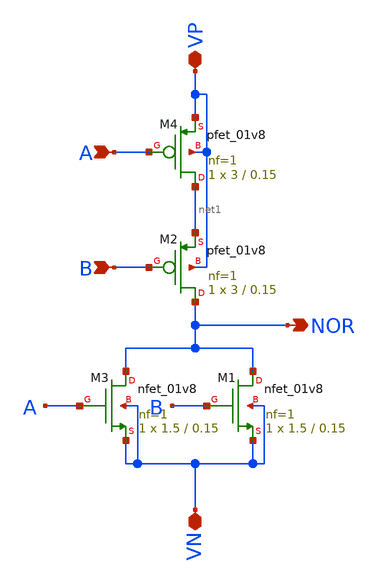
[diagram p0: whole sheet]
** sch_path: skywater_stuff/NOR_VP_VN_LVS.sch
**.subckt NOR_VP_VN_LVS A B NOR VP VN
*.ipin A
*.ipin B
*.opin NOR
*.iopin VP
*.iopin VN
XM1 NOR B VN VN sky130_fd_pr__nfet_01v8 L=0.15 W=1.5 nf=1 ad='int((nf+1)/2) * W/nf * 0.29' as='int((nf+2)/2) * W/nf * 0.29'
+ pd='2*int((nf+1)/2) * (W/nf + 0.29)' ps='2*int((nf+2)/2) * (W/nf + 0.29)' nrd='0.29 / W' nrs='0.29 / W'
+ sa=0 sb=0 sd=0 mult=1 m=1
XM3 NOR A VN VN sky130_fd_pr__nfet_01v8 L=0.15 W=1.5 nf=1 ad='int((nf+1)/2) * W/nf * 0.29' as='int((nf+2)/2) * W/nf * 0.29'
+ pd='2*int((nf+1)/2) * (W/nf + 0.29)' ps='2*int((nf+2)/2) * (W/nf + 0.29)' nrd='0.29 / W' nrs='0.29 / W'
+ sa=0 sb=0 sd=0 mult=1 m=1
XM4 net1 A VP VP sky130_fd_pr__pfet_01v8 L=0.15 W=3 nf=1 ad='int((nf+1)/2) * W/nf * 0.29' as='int((nf+2)/2) * W/nf * 0.29'
+ pd='2*int((nf+1)/2) * (W/nf + 0.29)' ps='2*int((nf+2)/2) * (W/nf + 0.29)' nrd='0.29 / W' nrs='0.29 / W'
+ sa=0 sb=0 sd=0 mult=1 m=1
XM2 NOR B net1 VP sky130_fd_pr__pfet_01v8 L=0.15 W=3 nf=1 ad='int((nf+1)/2) * W/nf * 0.29' as='int((nf+2)/2) * W/nf * 0.29'
+ pd='2*int((nf+1)/2) * (W/nf + 0.29)' ps='2*int((nf+2)/2) * (W/nf + 0.29)' nrd='0.29 / W' nrs='0.29 / W'
+ sa=0 sb=0 sd=0 mult=1 m=1
**.ends
.end
